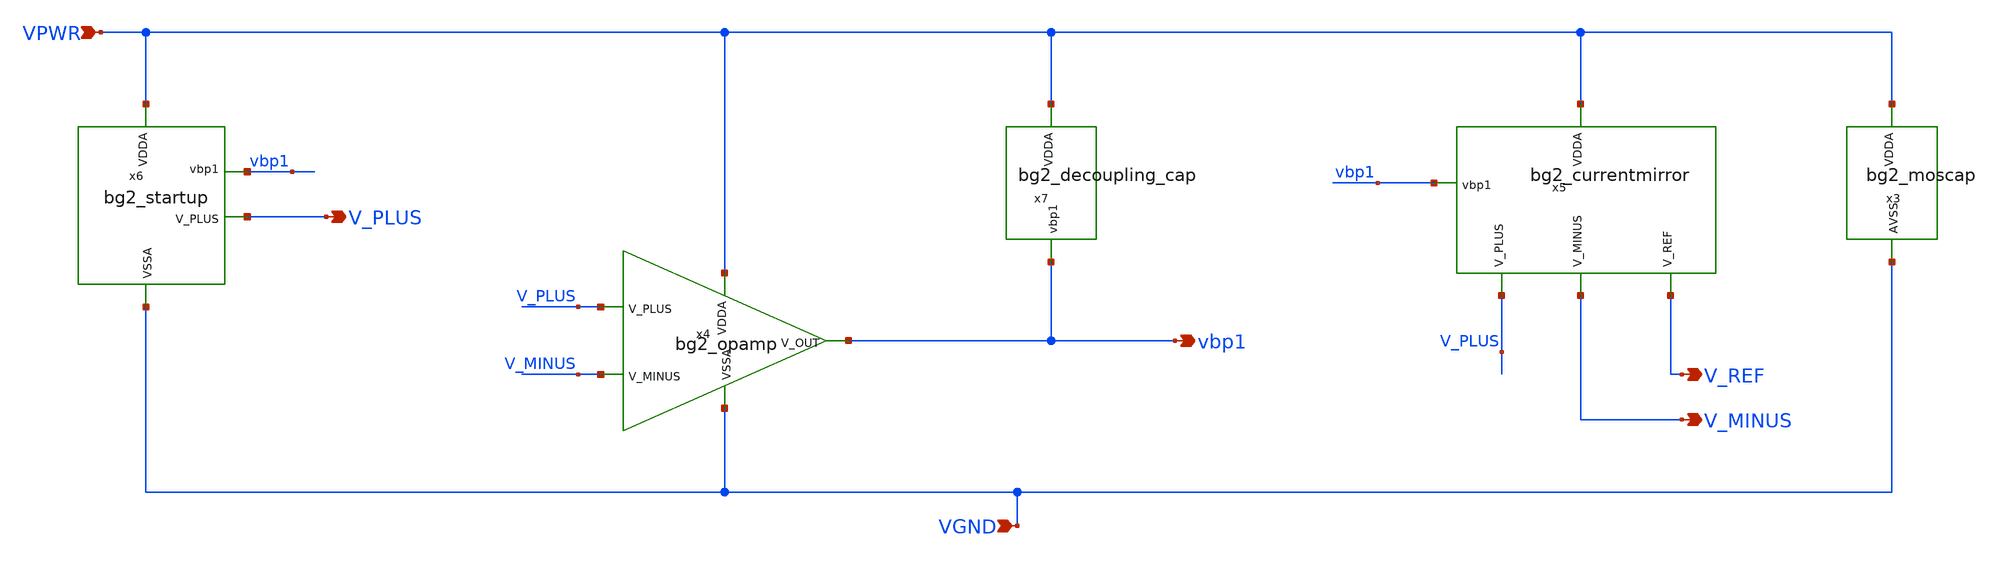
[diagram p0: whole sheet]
** sch_path: lef/lef/lef/gds/bg2_top_tt_v5.sch
**.subckt bg2_top_tt_v5 VGND VPWR vbp1 V_PLUS V_MINUS V_REF
*.ipin VGND
*.ipin VPWR
*.opin vbp1
*.opin V_PLUS
*.opin V_MINUS
*.opin V_REF
x3 VPWR VGND bg2_moscap
x7 VPWR vbp1 bg2_decoupling_cap
x6 VPWR vbp1 V_PLUS VGND bg2_startup
x5 VPWR vbp1 V_MINUS V_REF V_PLUS bg2_currentmirror
x4 VPWR vbp1 V_PLUS V_MINUS VGND bg2_opamp
**.ends
.end
